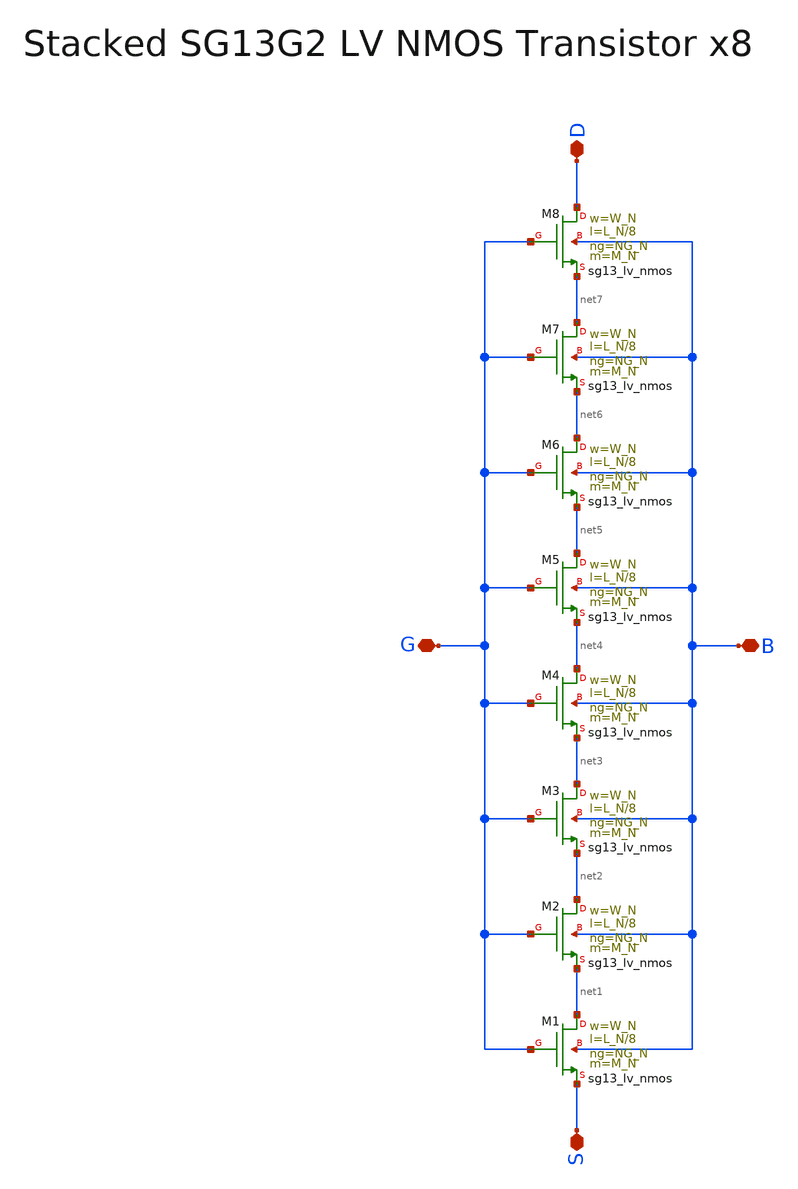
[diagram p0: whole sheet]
** sch_path: SG13G2_ATBS-ADC-main/xschem/stacked_transistors/sg13g2_lv_nmos_stacked/sg13g2_lv_nmos_stacked_x8.sch
**.subckt sg13g2_lv_nmos_stacked_x8 D S G B
*.iopin D
*.iopin S
*.iopin G
*.iopin B
XM1 net1 G S B sg13_lv_nmos w=W_N l=L_N/8 ng=NG_N m=M_N mm_ok=1
XM2 net2 G net1 B sg13_lv_nmos w=W_N l=L_N/8 ng=NG_N m=M_N mm_ok=1
XM3 net3 G net2 B sg13_lv_nmos w=W_N l=L_N/8 ng=NG_N m=M_N mm_ok=1
XM4 net4 G net3 B sg13_lv_nmos w=W_N l=L_N/8 ng=NG_N m=M_N mm_ok=1
XM5 net5 G net4 B sg13_lv_nmos w=W_N l=L_N/8 ng=NG_N m=M_N mm_ok=1
XM6 net6 G net5 B sg13_lv_nmos w=W_N l=L_N/8 ng=NG_N m=M_N mm_ok=1
XM7 net7 G net6 B sg13_lv_nmos w=W_N l=L_N/8 ng=NG_N m=M_N mm_ok=1
XM8 D G net7 B sg13_lv_nmos w=W_N l=L_N/8 ng=NG_N m=M_N mm_ok=1
**.ends
.end
